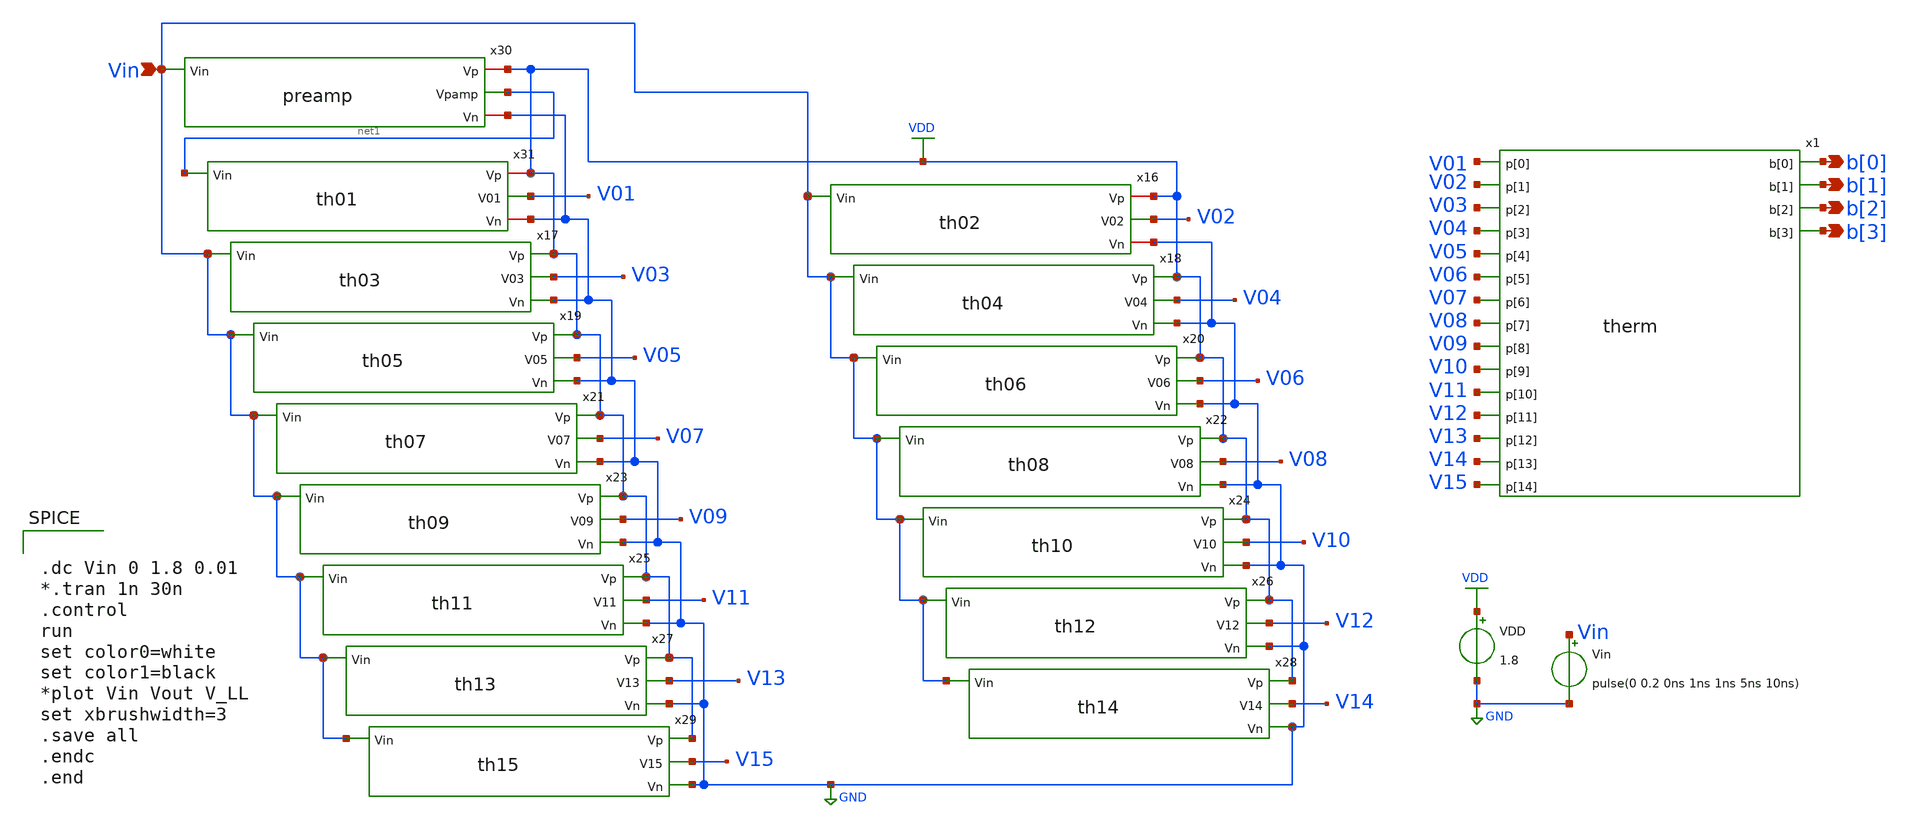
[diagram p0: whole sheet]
** sch_path: xschem/Vth_sch/Pre_layout/analog_therm.sch
**.subckt analog_therm b[0] Vin b[1] b[2] b[3]
*.opin b[0]
*.ipin Vin
*.opin b[1]
*.opin b[2]
*.opin b[3]
x16 VDD Vin V02 GND th02
x17 VDD V03 Vin GND th03
x18 VDD V04 Vin GND th04
x19 VDD V05 Vin GND th05
x20 VDD Vin V06 GND th06
x21 VDD Vin V07 GND th07
x22 VDD V08 Vin GND th08
x23 VDD V09 Vin GND th09
x24 VDD V10 Vin GND th10
x25 VDD V11 Vin GND th11
x26 VDD V12 Vin GND th12
x27 VDD V13 Vin GND th13
x28 VDD V14 Vin GND th14
x29 VDD V15 Vin GND th15
x30 VDD Vin net1 GND preamp
x31 VDD net1 V01 GND th01
x1 V01 V02 V03 b[0] V04 V05 b[1] V06 V07 V08 b[2] V09 V10 b[3] V11 V12 V13 V14 V15 therm
VDD VDD GND 1.8
Vin Vin GND pulse(0 0.2 0ns 1ns 1ns 5ns 10ns)
**** begin user architecture code


.dc Vin 0 1.8 0.01
*.tran 1n 30n
.control
run
set color0=white
set color1=black
*plot Vin Vout V_LL
set xbrushwidth=3
.save all
.endc
.end




.lib /usr/local/share/pdk/sky130A/libs.tech/ngspice/sky130.lib.spice tt
.include /usr/local/share/pdk/sky130A/libs.ref/sky130_fd_sc_hd/spice/sky130_fd_sc_hd.spice

.save all



**** end user architecture code
**.ends
.GLOBAL VDD
.GLOBAL GND
.end
